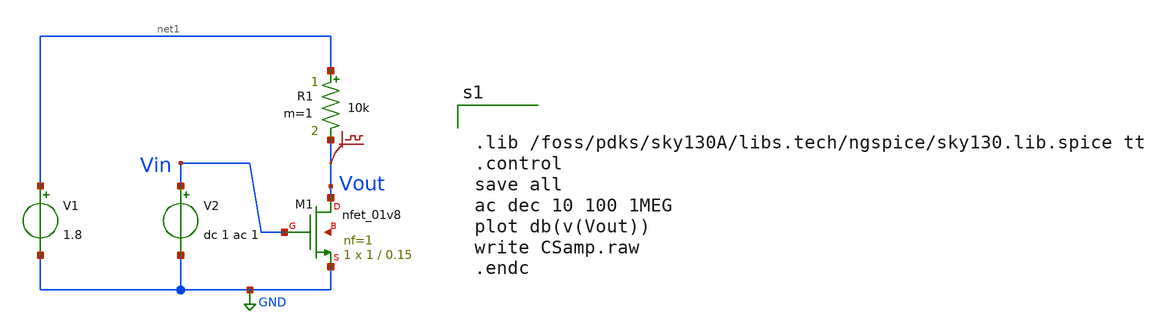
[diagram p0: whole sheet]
** sch_path: CSamp.sch
**.subckt CSamp
V1 net1 GND 1.8
V2 Vin GND dc 1 ac 1
R1 net1 Vout 10k m=1
XM1 Vout Vin GND net2 sky130_fd_pr__nfet_01v8 L=0.15 W=1 nf=1 ad='int((nf+1)/2) * W/nf * 0.29' as='int((nf+2)/2) * W/nf * 0.29'
+ pd='2*int((nf+1)/2) * (W/nf + 0.29)' ps='2*int((nf+2)/2) * (W/nf + 0.29)' nrd='0.29 / W' nrs='0.29 / W'
+ sa=0 sb=0 sd=0 mult=1 m=1
.save v(vout)
**** begin user architecture code


.lib /foss/pdks/sky130A/libs.tech/ngspice/sky130.lib.spice tt
.control
save all
ac dec 10 100 1MEG
plot db(v(Vout))
write CSamp.raw
.endc


**** end user architecture code
**.ends
.GLOBAL GND
.end
